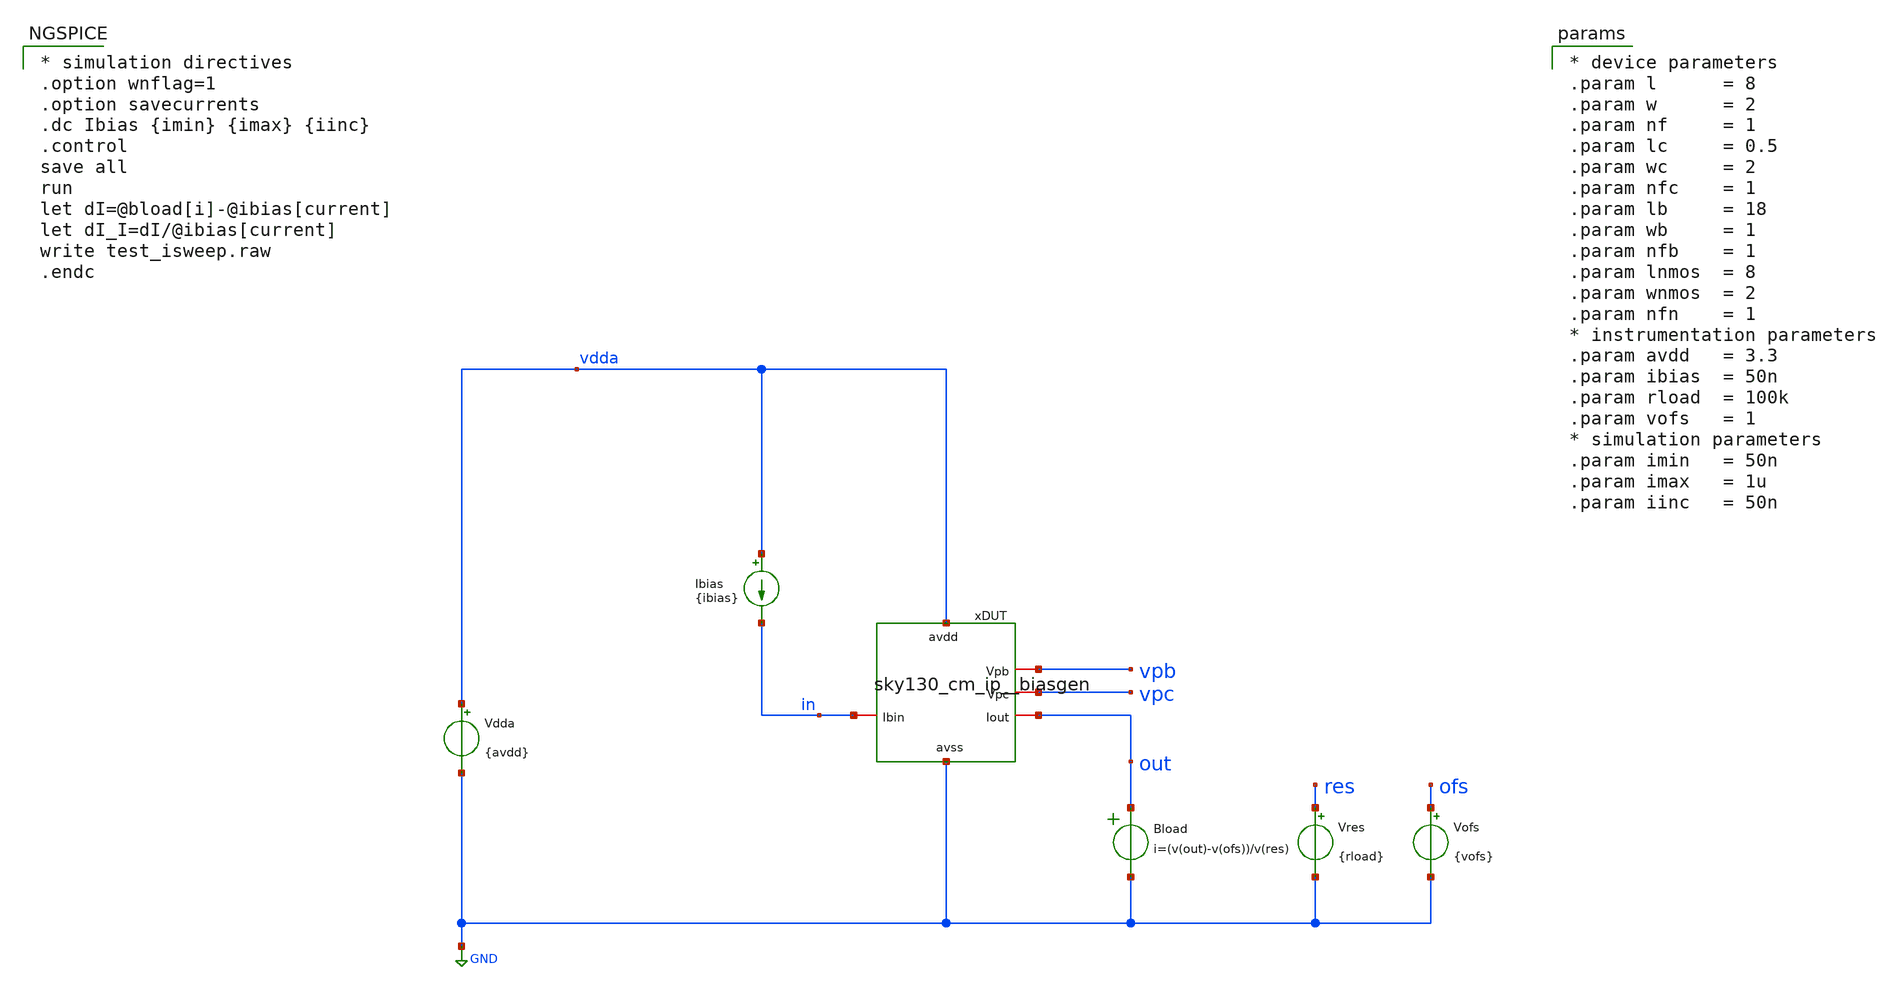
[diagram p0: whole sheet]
** sch_path: xschem/test_isweep.sch
**.subckt test_isweep
Vdda vdda GND {avdd}
.save i(vdda)
Ibias vdda in {ibias}
Vres res GND {rload}
Bload out GND i=(v(out)-v(ofs))/v(res)
Vofs ofs GND {vofs}
xDUT vdda vpb vpc out in GND sky130_cm_ip__biasgen l=8 w=2 nf=1 lc=0.5 wc=2 nfc=1 lb=18 wb=1 nfb=1
+ ln=8 wn=2 nfn=1
**** begin user architecture code

* device parameters
.param l      = 8
.param w      = 2
.param nf     = 1
.param lc     = 0.5
.param wc     = 2
.param nfc    = 1
.param lb     = 18
.param wb     = 1
.param nfb    = 1
.param lnmos  = 8
.param wnmos  = 2
.param nfn    = 1
* instrumentation parameters
.param avdd   = 3.3
.param ibias  = 50n
.param rload  = 100k
.param vofs   = 1
* simulation parameters
.param imin   = 50n
.param imax   = 1u
.param iinc   = 50n


** opencircuitdesign pdks install
.lib $::SKYWATER_MODELS/sky130.lib.spice tt



* simulation directives
.option wnflag=1
.option savecurrents
.dc Ibias {imin} {imax} {iinc}
.control
save all
run
let dI=@bload[i]-@ibias[current]
let dI_I=dI/@ibias[current]
write test_isweep.raw
.endc


**** end user architecture code
**.ends

* expanding   symbol:  xschem/sky130_cm_ip__biasgen.sym # of pins=6
** sym_path: xschem/sky130_cm_ip__biasgen.sym
** sch_path: xschem/sky130_cm_ip__biasgen.sch
.subckt sky130_cm_ip__biasgen avdd Vpb Vpc Iout Ibin avss  l=8 w=2 nf=1 lc=0.5 wc=2 nfc=1 lb=18 wb=1
+ nfb=1 lnmos=8 wnmos=2 nfnmos=1
*.iopin avss
*.iopin avdd
*.iopin Ibin
*.iopin Vpb
*.iopin Vpc
*.iopin Iout
XMc1 Vpb vpc1 vd1 avdd sky130_fd_pr__pfet_g5v0d10v5 L={lc} W={wc} nf={nfc} ad='int(({nfc} + 1)/2) * {wc} / {nfc} * 0.29'
+ as='int(({nfc} + 2)/2) * {wc} / {nfc} * 0.29' pd='2*int(({nfc} + 1)/2) * ({wc} / {nfc} + 0.29)' ps='2*int(({nfc} + 2)/2) * ({wc} / {nfc} + 0.29)'
+ nrd='0.29 / {wc} ' nrs='0.29 / {wc} ' sa=0 sb=0 sd=0 mult=1 m=1
XM1 vd1 Vpb avdd avdd sky130_fd_pr__pfet_g5v0d10v5 L={l} W={w} nf={nf} ad='int(({nf} + 1)/2) * {w} / {nf} * 0.29'
+ as='int(({nf} + 2)/2) * {w} / {nf} * 0.29' pd='2*int(({nf} + 1)/2) * ({w} / {nf} + 0.29)' ps='2*int(({nf} + 2)/2) * ({w} / {nf} + 0.29)'
+ nrd='0.29 / {w} ' nrs='0.29 / {w} ' sa=0 sb=0 sd=0 mult=1 m=1
XMc2 Iout vpc2 vd2 avdd sky130_fd_pr__pfet_g5v0d10v5 L={lc} W={wc} nf={nfc} ad='int(({nfc} + 1)/2) * {wc} / {nfc} * 0.29'
+ as='int(({nfc} + 2)/2) * {wc} / {nfc} * 0.29' pd='2*int(({nfc} + 1)/2) * ({wc} / {nfc} + 0.29)' ps='2*int(({nfc} + 2)/2) * ({wc} / {nfc} + 0.29)'
+ nrd='0.29 / {wc} ' nrs='0.29 / {wc} ' sa=0 sb=0 sd=0 mult=1 m=1
XM2 vd2 Vpb avdd avdd sky130_fd_pr__pfet_g5v0d10v5 L={l} W={w} nf={nf} ad='int(({nf} + 1)/2) * {w} / {nf} * 0.29'
+ as='int(({nf} + 2)/2) * {w} / {nf} * 0.29' pd='2*int(({nf} + 1)/2) * ({w} / {nf} + 0.29)' ps='2*int(({nf} + 2)/2) * ({w} / {nf} + 0.29)'
+ nrd='0.29 / {w} ' nrs='0.29 / {w} ' sa=0 sb=0 sd=0 mult=1 m=1
XMc3 Vpc Vpc avdd avdd sky130_fd_pr__pfet_g5v0d10v5 L={lb} W={wb} nf={nfb} ad='int(({nfb} + 1)/2) * {wb} / {nfb} * 0.29'
+ as='int(({nfb} + 2)/2) * {wb} / {nfb} * 0.29' pd='2*int(({nfb} + 1)/2) * ({wb} / {nfb} + 0.29)' ps='2*int(({nfb} + 2)/2) * ({wb} / {nfb} + 0.29)'
+ nrd='0.29 / {wb} ' nrs='0.29 / {wb} ' sa=0 sb=0 sd=0 mult=1 m=1
XMn1 Ibin Ibin avss avss sky130_fd_pr__nfet_g5v0d10v5 L={lnmos} W={wnmos} nf={nfnmos} ad='int(({nfnmos} + 1)/2) * {wnmos} / {nfnmos} * 0.29'
+ as='int(({nfnmos} + 2)/2) * {wnmos} / {nfnmos} * 0.29' pd='2*int(({nfnmos} + 1)/2) * ({wnmos} / {nfnmos} + 0.29)'
+ ps='2*int(({nfnmos} + 2)/2) * ({wnmos} / {nfnmos} + 0.29)' nrd='0.29 / {wnmos} ' nrs='0.29 / {wnmos} '
+ sa=0 sb=0 sd=0 mult=1 m=1
XMn2 Vpc Ibin avss avss sky130_fd_pr__nfet_g5v0d10v5 L={lnmos} W={wnmos} nf={nfnmos} ad='int(({nfnmos} + 1)/2) * {wnmos} / {nfnmos} * 0.29'
+ as='int(({nfnmos} + 2)/2) * {wnmos} / {nfnmos} * 0.29' pd='2*int(({nfnmos} + 1)/2) * ({wnmos} / {nfnmos} + 0.29)'
+ ps='2*int(({nfnmos} + 2)/2) * ({wnmos} / {nfnmos} + 0.29)' nrd='0.29 / {wnmos} ' nrs='0.29 / {wnmos} '
+ sa=0 sb=0 sd=0 mult=1 m=1
XMn3 Vpb Ibin avss avss sky130_fd_pr__nfet_g5v0d10v5 L={lnmos} W={wnmos} nf={nfnmos} ad='int(({nfnmos} + 1)/2) * {wnmos} / {nfnmos} * 0.29'
+ as='int(({nfnmos} + 2)/2) * {wnmos} / {nfnmos} * 0.29' pd='2*int(({nfnmos} + 1)/2) * ({wnmos} / {nfnmos} + 0.29)'
+ ps='2*int(({nfnmos} + 2)/2) * ({wnmos} / {nfnmos} + 0.29)' nrd='0.29 / {wnmos} ' nrs='0.29 / {wnmos} '
+ sa=0 sb=0 sd=0 mult=1 m=1
XMon1 Vpc avss vpc1 avdd sky130_fd_pr__pfet_g5v0d10v5 L=.5 W=1 nf=1 ad='int((1 + 1)/2) * 1 / 1 * 0.29'
+ as='int((1 + 2)/2) * 1 / 1 * 0.29' pd='2*int((1 + 1)/2) * (1 / 1 + 0.29)' ps='2*int((1 + 2)/2) * (1 / 1 + 0.29)'
+ nrd='0.29 / 1 ' nrs='0.29 / 1 ' sa=0 sb=0 sd=0 mult=1 m=1
XMoff1 vpc1 avdd avdd avdd sky130_fd_pr__pfet_g5v0d10v5 L=.5 W=1 nf=1 ad='int((1 + 1)/2) * 1 / 1 * 0.29'
+ as='int((1 + 2)/2) * 1 / 1 * 0.29' pd='2*int((1 + 1)/2) * (1 / 1 + 0.29)' ps='2*int((1 + 2)/2) * (1 / 1 + 0.29)'
+ nrd='0.29 / 1 ' nrs='0.29 / 1 ' sa=0 sb=0 sd=0 mult=1 m=1
XMon2 Vpc avss vpc2 avdd sky130_fd_pr__pfet_g5v0d10v5 L=.5 W=1 nf=1 ad='int((1 + 1)/2) * 1 / 1 * 0.29'
+ as='int((1 + 2)/2) * 1 / 1 * 0.29' pd='2*int((1 + 1)/2) * (1 / 1 + 0.29)' ps='2*int((1 + 2)/2) * (1 / 1 + 0.29)'
+ nrd='0.29 / 1 ' nrs='0.29 / 1 ' sa=0 sb=0 sd=0 mult=1 m=1
XMoff2 vpc2 avdd avdd avdd sky130_fd_pr__pfet_g5v0d10v5 L=.5 W=1 nf=1 ad='int((1 + 1)/2) * 1 / 1 * 0.29'
+ as='int((1 + 2)/2) * 1 / 1 * 0.29' pd='2*int((1 + 1)/2) * (1 / 1 + 0.29)' ps='2*int((1 + 2)/2) * (1 / 1 + 0.29)'
+ nrd='0.29 / 1 ' nrs='0.29 / 1 ' sa=0 sb=0 sd=0 mult=1 m=1
.ends

.GLOBAL GND
.end
